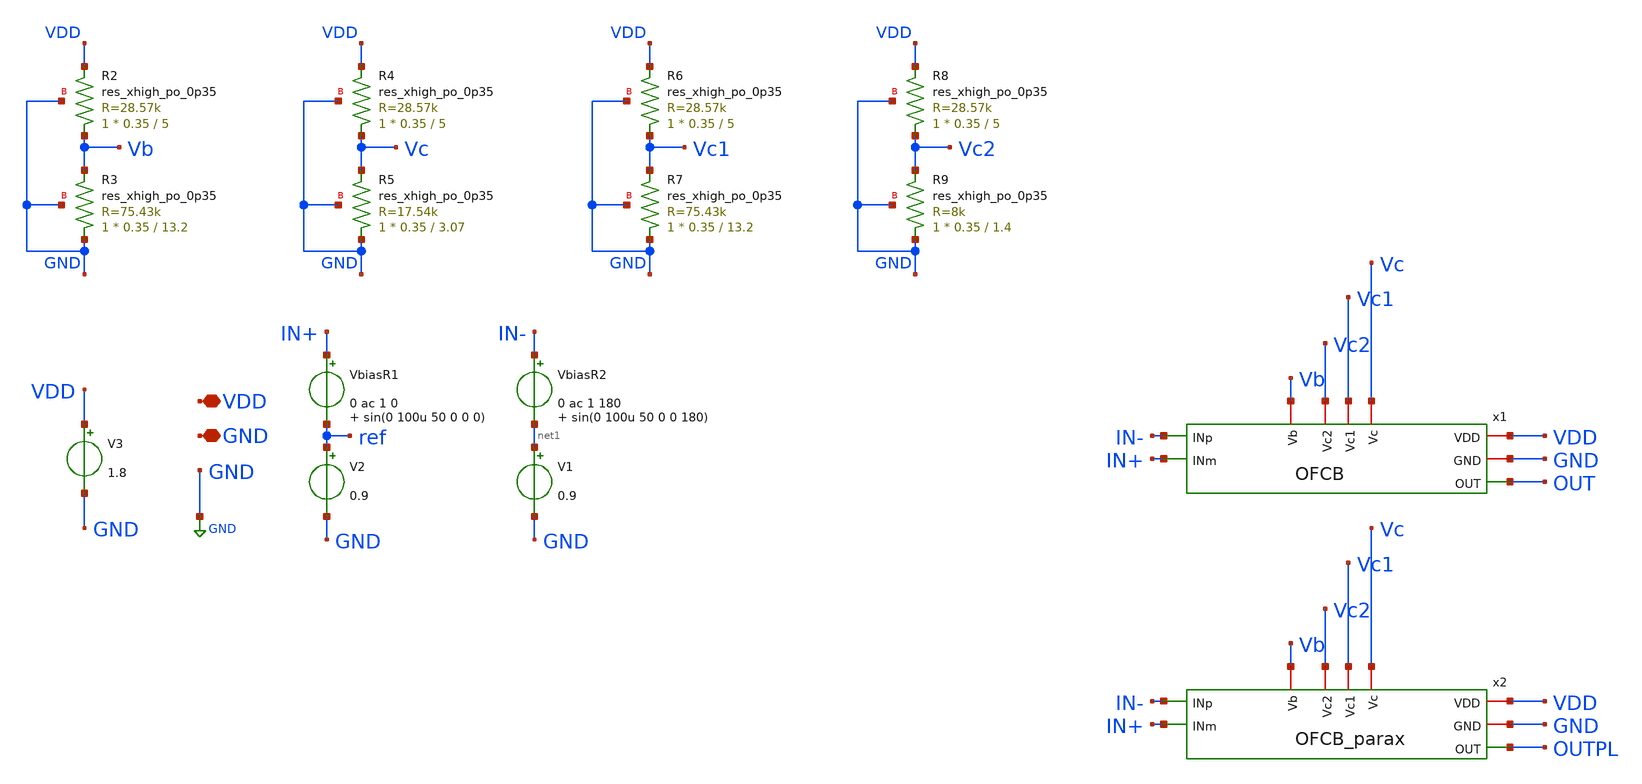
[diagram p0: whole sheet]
** sch_path: xschem/OFCBPL.sch
**.subckt OFCBPL VDD GND
*.iopin VDD
*.iopin GND
x1 Vb VDD GND Vc2 OUT IN- IN+ Vc1 Vc OFCB
x2 Vb VDD GND Vc2 OUTPL IN- IN+ Vc1 Vc OFCB_parax
VbiasR1 IN+ ref 0 ac 1 0 sin(0 100u 50 0 0 0)
V2 ref GND 0.9
V3 VDD GND 1.8
XR2 Vb VDD GND sky130_fd_pr__res_xhigh_po_0p35 L=5 mult=1 m=1
XR3 GND Vb GND sky130_fd_pr__res_xhigh_po_0p35 L=13.2 mult=1 m=1
XR4 Vc VDD GND sky130_fd_pr__res_xhigh_po_0p35 L=5 mult=1 m=1
XR5 GND Vc GND sky130_fd_pr__res_xhigh_po_0p35 L=3.07 mult=1 m=1
XR6 Vc1 VDD GND sky130_fd_pr__res_xhigh_po_0p35 L=5 mult=1 m=1
XR7 GND Vc1 GND sky130_fd_pr__res_xhigh_po_0p35 L=13.2 mult=1 m=1
XR8 Vc2 VDD GND sky130_fd_pr__res_xhigh_po_0p35 L=5 mult=1 m=1
XR9 GND Vc2 GND sky130_fd_pr__res_xhigh_po_0p35 L=1.4 mult=1 m=1
VbiasR2 IN- net1 0 ac 1 180 sin(0 100u 50 0 0 180)
V1 net1 GND 0.9
**** begin user architecture code



.control
    set wr_vecnames
    set wr_singlescale

    let mc_runs = 5
    let run = 1

    dowhile run <= mc_runs
        * Punto di lavoro
        op

        * Analisi AC (Frequenza)
        ac dec 10 1 100meg

        * Analisi Transitoria (Tempo)
        tran 100u 100m

        reset

        let run = run + 1
    end

    * --- GRAFICO AC (Asse X in Frequenza) ---
    * Passiamo al plot AC per impostare la scala logaritmica corretta
    setplot ac1
    plot db(ac1.v(OUT)) db(ac2.v(OUT)) db(ac3.v(OUT)) db(ac4.v(OUT)) db(ac5.v(OUT)) title 'AC Gain Response (Frequency)'
    plot db(ac1.v(OUTPL)) db(ac2.v(OUTPL)) db(ac3.v(OUTPL)) db(ac4.v(OUTPL)) db(ac5.v(OUTPL))
    * --- GRAFICO TRAN (Asse X in Tempo) ---
    * Passiamo al plot TRAN per impostare la scala temporale
    setplot tran1
    plot tran1.v(OUT) tran2.v(OUT) tran3.v(OUT) tran4.v(OUT) tran5.v(OUT) title 'Transient Response (Time)'

.endc



.lib $::SKYWATER_MODELS/sky130.lib.spice tt_mm
**** end user architecture code
**.ends

* expanding   symbol:  OFCB.sym # of pins=9
** sym_path: xschem/OFCB.sym
** sch_path: xschem/OFCB.sch
.subckt OFCB Vb VDD GND Vc2 OUT INp INm Vc1 Vc
*.iopin VDD
*.iopin GND
*.opin OUT
*.ipin INp
*.ipin INm
*.iopin Vc2
*.iopin Vc1
*.iopin Vc
*.iopin Vb
XM11 S Vb VDD VDD sky130_fd_pr__pfet_01v8_lvt L=1 W=60 nf=1 ad='int((nf+1)/2) * W/nf * 0.29' as='int((nf+2)/2) * W/nf * 0.29'
+ pd='2*int((nf+1)/2) * (W/nf + 0.29)' ps='2*int((nf+2)/2) * (W/nf + 0.29)' nrd='0.29 / W' nrs='0.29 / W'
+ sa=0 sb=0 sd=0 mult=2 m=2
XM1 D1 INp S S sky130_fd_pr__pfet_01v8_lvt L=10 W=25 nf=2 ad='int((nf+1)/2) * W/nf * 0.29' as='int((nf+2)/2) * W/nf * 0.29'
+ pd='2*int((nf+1)/2) * (W/nf + 0.29)' ps='2*int((nf+2)/2) * (W/nf + 0.29)' nrd='0.29 / W' nrs='0.29 / W'
+ sa=0 sb=0 sd=0 mult=2 m=2
XM2 D2 INm S S sky130_fd_pr__pfet_01v8_lvt L=10 W=25 nf=2 ad='int((nf+1)/2) * W/nf * 0.29' as='int((nf+2)/2) * W/nf * 0.29'
+ pd='2*int((nf+1)/2) * (W/nf + 0.29)' ps='2*int((nf+2)/2) * (W/nf + 0.29)' nrd='0.29 / W' nrs='0.29 / W'
+ sa=0 sb=0 sd=0 mult=2 m=2
XM3 OUT Vc1 D2 GND sky130_fd_pr__nfet_01v8_lvt L=1 W=4 nf=1 ad='int((nf+1)/2) * W/nf * 0.29' as='int((nf+2)/2) * W/nf * 0.29'
+ pd='2*int((nf+1)/2) * (W/nf + 0.29)' ps='2*int((nf+2)/2) * (W/nf + 0.29)' nrd='0.29 / W' nrs='0.29 / W'
+ sa=0 sb=0 sd=0 mult=1 m=1
XM4 D2 Vc GND GND sky130_fd_pr__nfet_01v8_lvt L=1 W=2.8 nf=1 ad='int((nf+1)/2) * W/nf * 0.29' as='int((nf+2)/2) * W/nf * 0.29'
+ pd='2*int((nf+1)/2) * (W/nf + 0.29)' ps='2*int((nf+2)/2) * (W/nf + 0.29)' nrd='0.29 / W' nrs='0.29 / W'
+ sa=0 sb=0 sd=0 mult=1 m=1
XM5 D1 Vc GND GND sky130_fd_pr__nfet_01v8_lvt L=1 W=2.8 nf=1 ad='int((nf+1)/2) * W/nf * 0.29' as='int((nf+2)/2) * W/nf * 0.29'
+ pd='2*int((nf+1)/2) * (W/nf + 0.29)' ps='2*int((nf+2)/2) * (W/nf + 0.29)' nrd='0.29 / W' nrs='0.29 / W'
+ sa=0 sb=0 sd=0 mult=1 m=1
XM6 G Vc1 D1 GND sky130_fd_pr__nfet_01v8_lvt L=1 W=4 nf=1 ad='int((nf+1)/2) * W/nf * 0.29' as='int((nf+2)/2) * W/nf * 0.29'
+ pd='2*int((nf+1)/2) * (W/nf + 0.29)' ps='2*int((nf+2)/2) * (W/nf + 0.29)' nrd='0.29 / W' nrs='0.29 / W'
+ sa=0 sb=0 sd=0 mult=1 m=1
XM7 G Vc2 D9 D9 sky130_fd_pr__pfet_01v8_lvt L=2.23 W=5 nf=1 ad='int((nf+1)/2) * W/nf * 0.29' as='int((nf+2)/2) * W/nf * 0.29'
+ pd='2*int((nf+1)/2) * (W/nf + 0.29)' ps='2*int((nf+2)/2) * (W/nf + 0.29)' nrd='0.29 / W' nrs='0.29 / W'
+ sa=0 sb=0 sd=0 mult=1 m=1
XM9 D9 G VDD VDD sky130_fd_pr__pfet_01v8_lvt L=2.23 W=3.8 nf=1 ad='int((nf+1)/2) * W/nf * 0.29' as='int((nf+2)/2) * W/nf * 0.29'
+ pd='2*int((nf+1)/2) * (W/nf + 0.29)' ps='2*int((nf+2)/2) * (W/nf + 0.29)' nrd='0.29 / W' nrs='0.29 / W'
+ sa=0 sb=0 sd=0 mult=1 m=1
XM8 D10 G VDD VDD sky130_fd_pr__pfet_01v8_lvt L=2.23 W=3.8 nf=1 ad='int((nf+1)/2) * W/nf * 0.29' as='int((nf+2)/2) * W/nf * 0.29'
+ pd='2*int((nf+1)/2) * (W/nf + 0.29)' ps='2*int((nf+2)/2) * (W/nf + 0.29)' nrd='0.29 / W' nrs='0.29 / W'
+ sa=0 sb=0 sd=0 mult=1 m=1
XM10 OUT Vc2 D10 D10 sky130_fd_pr__pfet_01v8_lvt L=2.23 W=5 nf=1 ad='int((nf+1)/2) * W/nf * 0.29' as='int((nf+2)/2) * W/nf * 0.29'
+ pd='2*int((nf+1)/2) * (W/nf + 0.29)' ps='2*int((nf+2)/2) * (W/nf + 0.29)' nrd='0.29 / W' nrs='0.29 / W'
+ sa=0 sb=0 sd=0 mult=1 m=1
XC1 OUT D1 sky130_fd_pr__cap_mim_m3_1 W=50 L=20 MF=1 m=1
.ends


* expanding   symbol:  OFCB_parax.sym # of pins=9
** sym_path: xschem/OFCB.sym
.include [file normalize ../mag/OFCB.sim.spice]
.GLOBAL GND
.end
